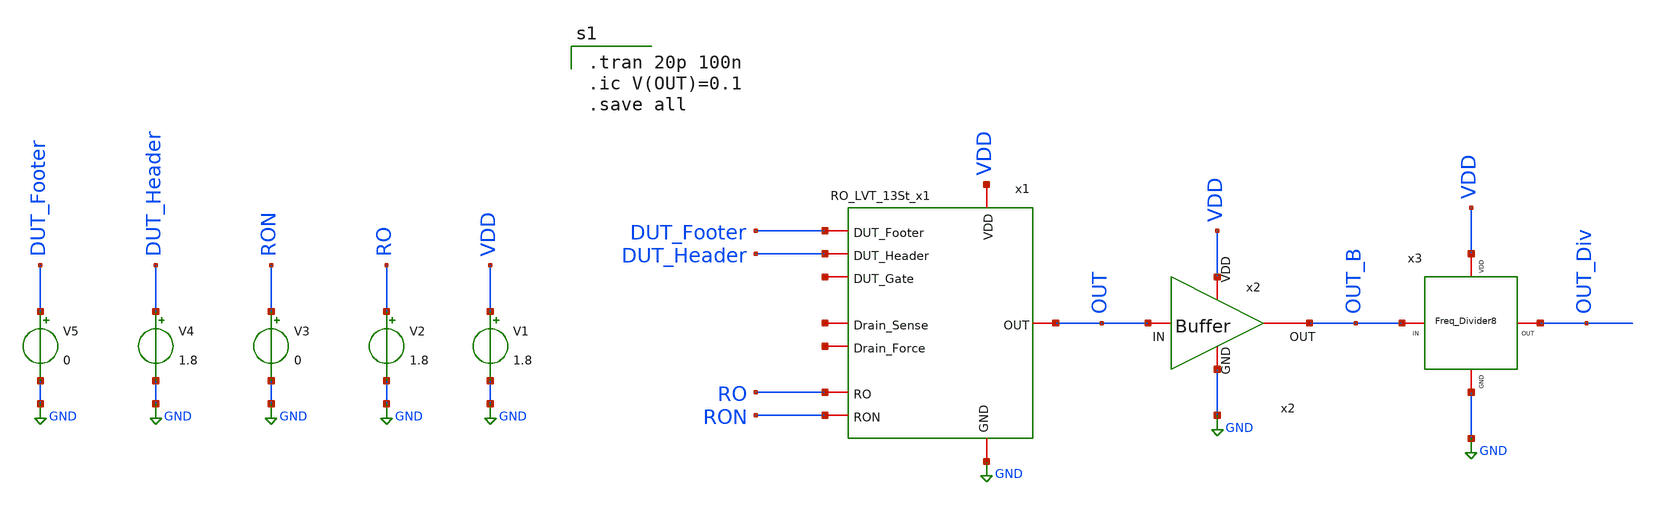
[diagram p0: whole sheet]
** sch_path: TB/13St_TB.sch
.lib $::SKYWATER_MODELS/sky130.lib.spice tt
.include $::SKYWATER_STDCELLS/sky130_fd_sc_hd.spice

**.subckt 13St_TB
V1 VDD GND 1.8
V2 RO GND 1.8
V3 RON GND 0
V4 DUT_Header GND 1.8
V5 DUT_Footer GND 0
x2 VDD OUT OUT_B GND Buffer
x3 OUT_B OUT_Div VDD GND Freq_Divider8
x1 VDD GND DUT_Footer DUT_Header net1 net2 RO RON net3 OUT RO_LVT_13St_x1
**** begin user architecture code

.tran 20p 100n
.ic V(OUT)=0.1
.save all

**** end user architecture code
**.ends
.GLOBAL GND
.GLOBAL VDD
.end
